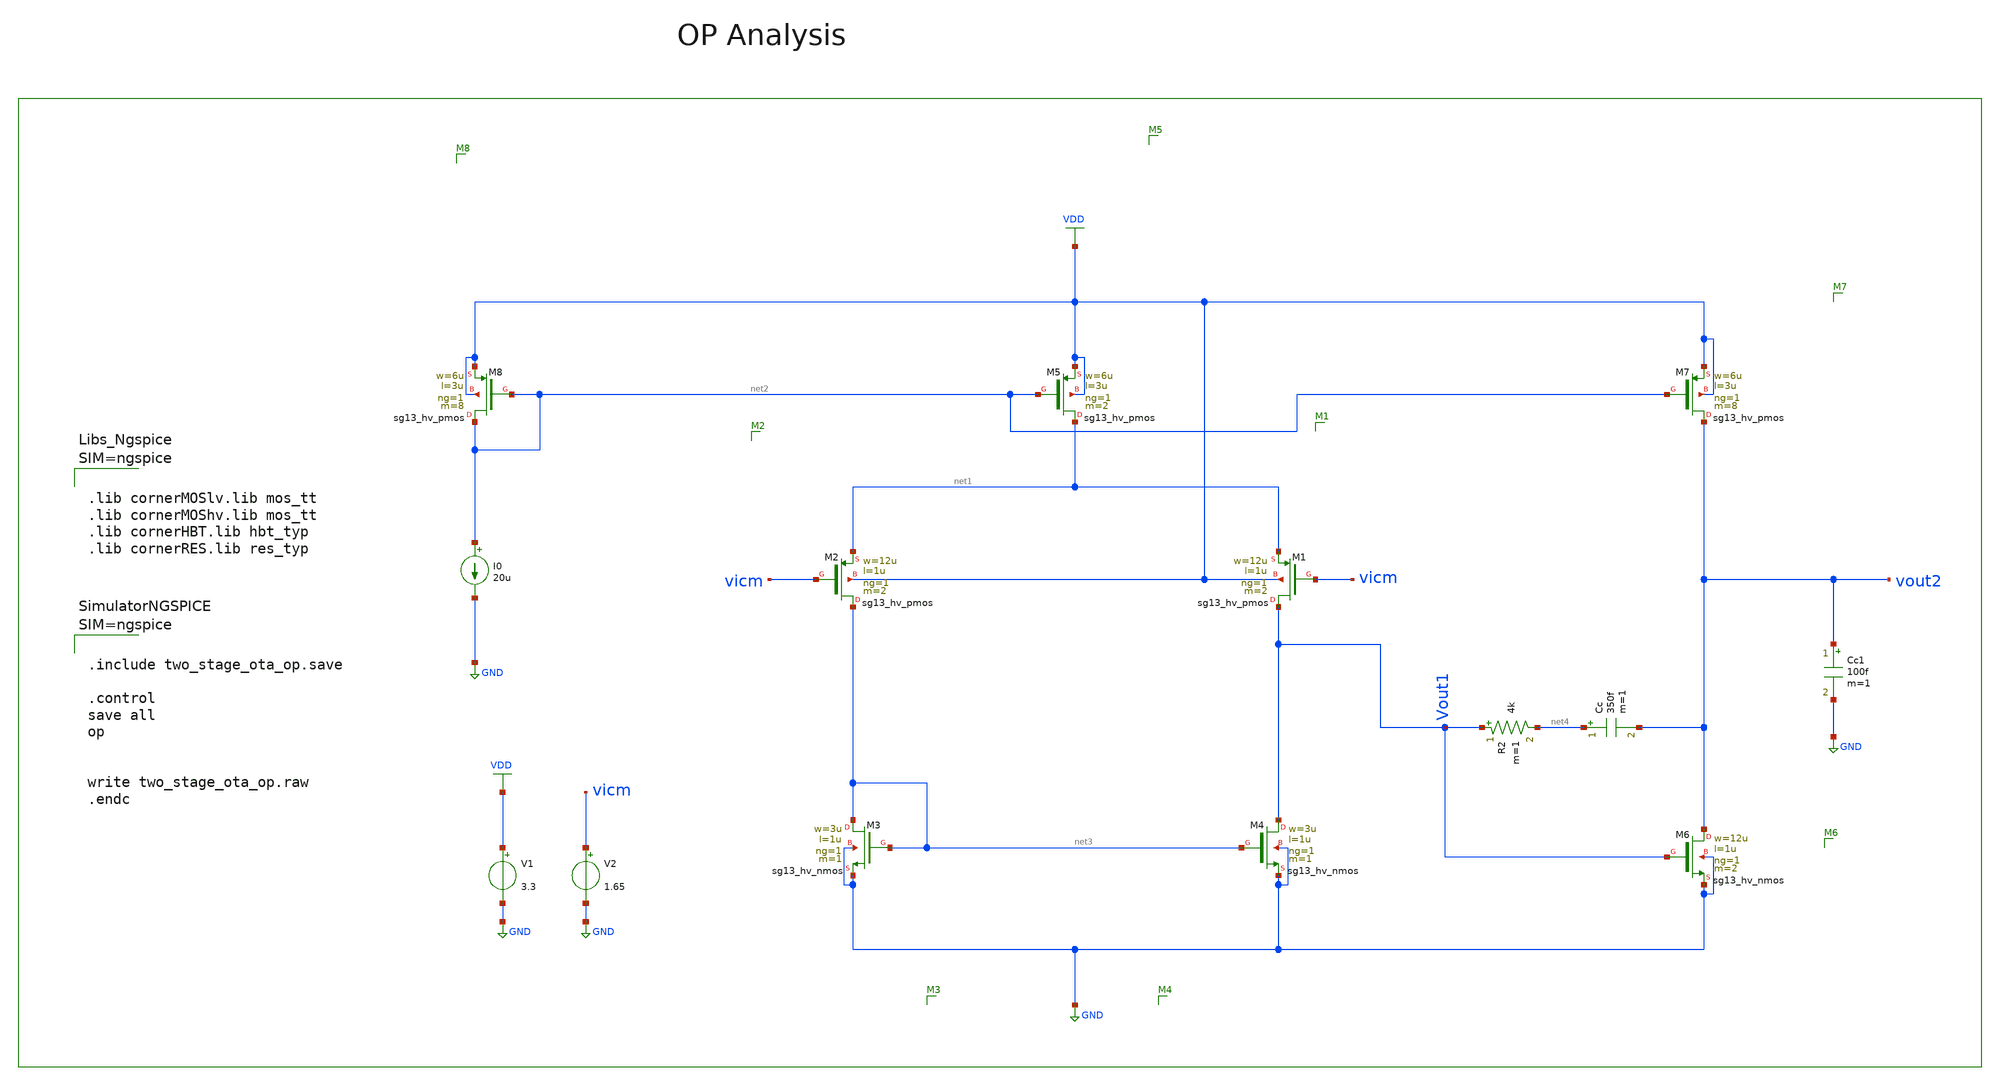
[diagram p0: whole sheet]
** sch_path: dependencies/pmu_ip/dependencies/OTA/OTA-main/testbenches/two_stage_ota_op.sch
* (c) 2025-2026 Ider Abdelaziz
**.subckt two_stage_ota_op
XM1 Vout1 vicm net1 VDD sg13_hv_pmos w=12u l=1u ng=1 m=2 mm_ok=1
XM2 net3 vicm net1 VDD sg13_hv_pmos w=12u l=1u ng=1 m=2 mm_ok=1
XM5 net1 net2 VDD VDD sg13_hv_pmos w=6u l=3u ng=1 m=2 mm_ok=1
XM3 net3 net3 GND GND sg13_hv_nmos w=3u l=1u ng=1 m=1 mm_ok=1
XM4 Vout1 net3 GND GND sg13_hv_nmos w=3u l=1u ng=1 m=1 mm_ok=1
XM7 vout2 net2 VDD VDD sg13_hv_pmos w=6u l=3u ng=1 m=8 mm_ok=1
XM6 vout2 Vout1 GND GND sg13_hv_nmos w=12u l=1u ng=1 m=2 mm_ok=1
Cc net4 vout2 350f m=1
Cc1 vout2 GND 100f m=1
V1 VDD GND 3.3
V2 vicm GND 1.65
R2 Vout1 net4 4k m=1
XM8 net2 net2 VDD VDD sg13_hv_pmos w=6u l=3u ng=1 m=8 mm_ok=1
I0 net2 GND 20u
**** begin user architecture code



.lib cornerMOSlv.lib mos_tt
.lib cornerMOShv.lib mos_tt
.lib cornerHBT.lib hbt_typ
.lib cornerRES.lib res_typ






.include two_stage_ota_op.save

.control
save all
op


write two_stage_ota_op.raw
.endc



**** end user architecture code
**.ends
.GLOBAL VDD
.GLOBAL GND
.end
